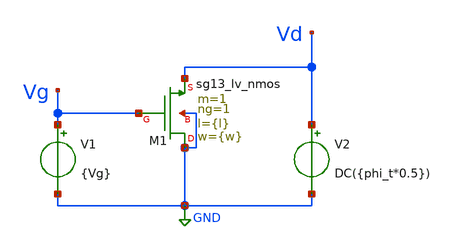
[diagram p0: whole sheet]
** sch_path: Parametros_Psp/VTH_test_v2.sch
**.subckt VTH_test_v2
V1 Vg GND {Vg}
V2 Vd GND DC({phi_t*0.5})
XM1 GND Vg Vd GND sg13_lv_nmos w={w} l={l} ng=1 m=1 mm_ok=1
**** begin user architecture code


* Circuit Parameters
.param vg = 3
.param step = 0.01
.param phi_t = 0.0258
.param w = 5.0u
.param l = 0.18u
* Include Models
.lib /opt/pdks/ihp-sg13g2/libs.tech/ngspice/models/cornerMOSlv.lib mos_tt
.lib /opt/pdks/ihp-sg13g2/libs.tech/ngspice/models/cornerMOShv.lib mos_tt
* OP Parameters & Singals to save
.save all
.save @n.xm1.nsg13_lv_nmos[ide]
.save @n.xm1.nsg13_lv_nmos[gm]
.save @n.xm1.nsg13_lv_nmos[vgs]
.save @n.xm1.nsg13_lv_nmos[vsb]
*Simulations
.dc V1 0 {vg} {step}
.control
run
show
setplot dc1save diff
plot -i(V2) @n.xm1.nsg13_lv_nmos[ide]
set filetype = ascii
write dcsweep_v2.raw
.endc
.end


**** end user architecture code
**.ends
.GLOBAL GND
.end
